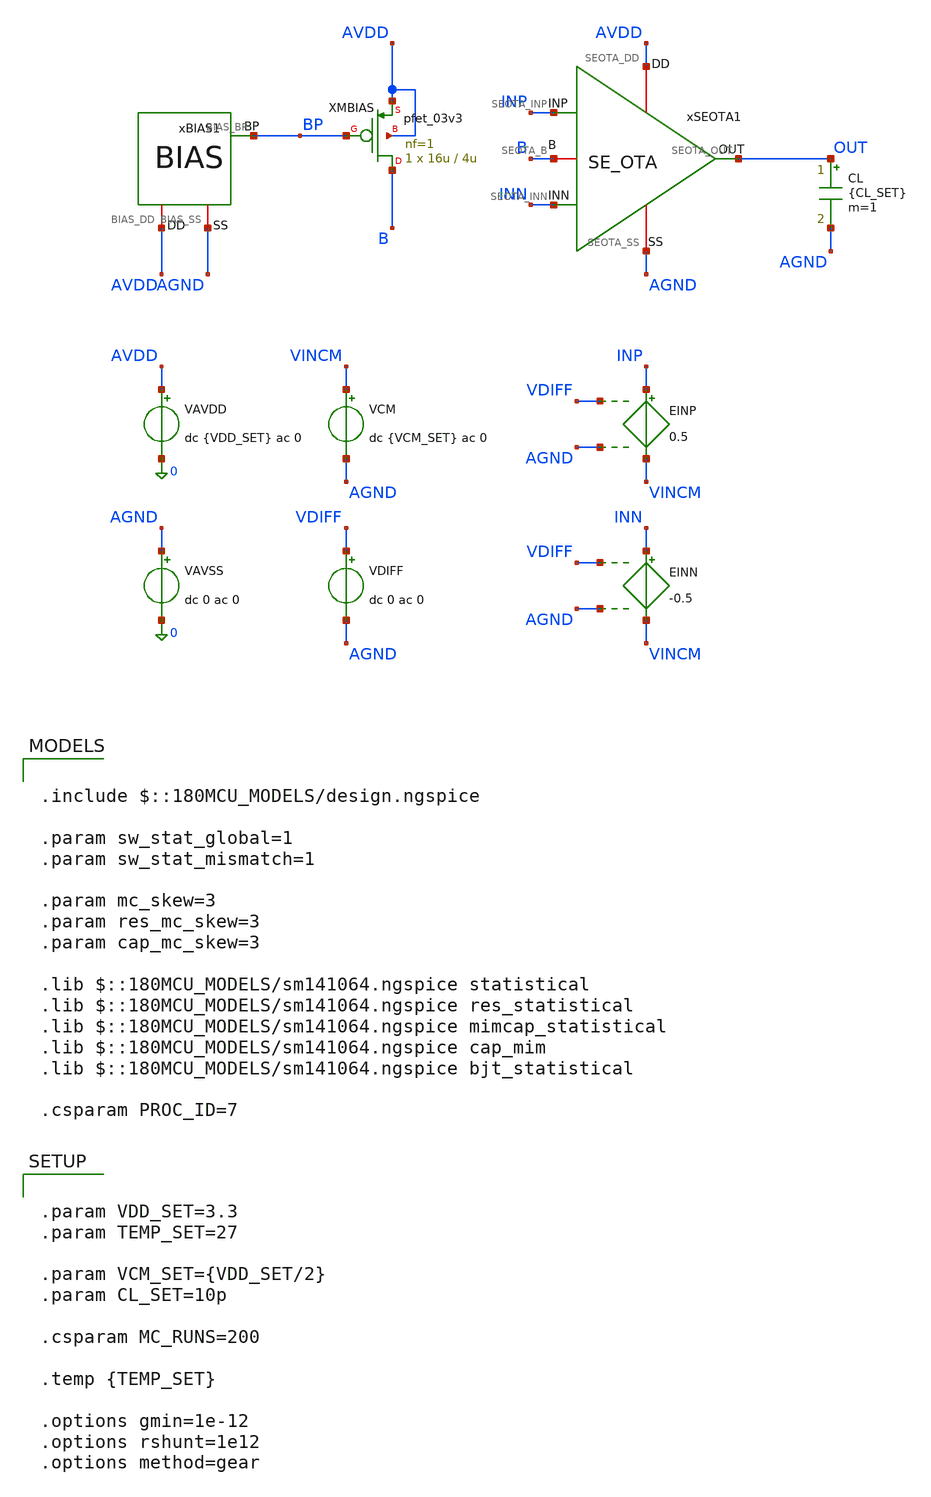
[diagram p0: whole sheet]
** sch_path: Design_Files/IC Design/Testbench/ANALOG_BLOCKS/SE_OTA/Open_Loop/SE_OTA_TB_OL_FULL.sch
**.subckt SE_OTA_TB_OL_FULL
VAVDD AVDD 0 dc {VDD_SET} ac 0
.save i(vavdd)
CL OUT AGND {CL_SET} m=1
VCM VINCM AGND dc {VCM_SET} ac 0
VDIFF VDIFF AGND dc 0 ac 0
xSEOTA1 AVDD AGND INP INN OUT B SE_OTA
VAVSS AGND 0 dc 0 ac 0
EINN INN VINCM VDIFF AGND -0.5
EINP INP VINCM VDIFF AGND 0.5
xBIAS1 AVDD AGND BP BIAS
XMBIAS B BP AVDD AVDD pfet_03v3 L=4u W=16u nf=1 ad='int((nf+1)/2) * W/nf * 0.18u' as='int((nf+2)/2) * W/nf * 0.18u'
+ pd='2*int((nf+1)/2) * (W/nf + 0.18u)' ps='2*int((nf+2)/2) * (W/nf + 0.18u)' nrd='0.18u / W' nrs='0.18u / W'
+ sa=0 sb=0 sd=0 m=1
**** begin user architecture code

.include $::180MCU_MODELS/design.ngspice

.param sw_stat_global=1
.param sw_stat_mismatch=1

.param mc_skew=3
.param res_mc_skew=3
.param cap_mc_skew=3

.lib $::180MCU_MODELS/sm141064.ngspice statistical
.lib $::180MCU_MODELS/sm141064.ngspice res_statistical
.lib $::180MCU_MODELS/sm141064.ngspice mimcap_statistical
.lib $::180MCU_MODELS/sm141064.ngspice cap_mim
.lib $::180MCU_MODELS/sm141064.ngspice bjt_statistical

.csparam PROC_ID=7




.control

destroy all

set noaskquit
set wr_singlescale
unset wr_vecnames

option klu
option numdgt=15
option method=gear
option maxord=2
option plotwinsize=0


if $&PROC_ID = 5
set proc=MM
else
if $&PROC_ID = 6
set proc=GL
else
set proc=FULL
end
end


shell mkdir -p /foss/designs/ECG_Acquisition_IC/Measurement_Results/IC_Simulation/ANALOG_BLOCKS/SE_OTA/{$proc}.Result_txt

shell rm -f /foss/designs/ECG_Acquisition_IC/Measurement_Results/IC_Simulation/ANALOG_BLOCKS/SE_OTA/{$proc}.Result_txt/{$proc}.ol_mc_summary.txt
shell rm -f /foss/designs/ECG_Acquisition_IC/Measurement_Results/IC_Simulation/ANALOG_BLOCKS/SE_OTA/{$proc}.Result_txt/{$proc}.ol_mc_debug_op.txt


echo run vos_V center_error_V ol_gain_1Hz ol_gain_dB ugf_Hz phase_ugf_deg pm_deg vout_center_V b_V ibias_A
+ idd_A power_W > /foss/designs/ECG_Acquisition_IC/Measurement_Results/IC_Simulation/ANALOG_BLOCKS/SE_OTA/{$proc}.Result_txt/{$proc}.ol_mc_summary.txt

echo run vos_V vout_zero_V vout_center_V center_error_V net1_V net2_V net3_V net4_V b_V ibias_A idd_A
+ power_W > /foss/designs/ECG_Acquisition_IC/Measurement_Results/IC_Simulation/ANALOG_BLOCKS/SE_OTA/{$proc}.Result_txt/{$proc}.ol_mc_debug_op.txt


let run=1
let mc_runs=$&MC_RUNS


dowhile run <= mc_runs


set runnum=$&run

setseed $runnum
mc_source


option klu
option numdgt=15
option method=gear
option maxord=2
option plotwinsize=0


* DEFAULT VALUES

set vos_val=0
set vout_zero_val=0
set vout_center_val=0
set center_error_val=0

set gain_val=0
set gain_db_val=0
set ugf_val=0
set phase_val=0
set pm_val=0

set net1_val=0
set net2_val=0
set net3_val=0
set net4_val=0

set b_val=0
set ibias_val=0
set idd_val=0
set power_val=0


* INITIAL SOURCES

alter @VCM[DC]=1.65
alter @VDIFF[DC]=0

alter @VCM[ACMAG]=0
alter @VDIFF[ACMAG]=0
alter @VAVDD[ACMAG]=0
alter @VAVSS[ACMAG]=0


save all
save @m.xmbias.m0[id]


* ZERO-DIFFERENTIAL OP

op

let vout_zero=v(OUT)-v(AGND)

set vout_zero_val=$&vout_zero


destroy all


* FIND OFFSET

alter @VDIFF[DC]=0

dc VDIFF -50m 50m 10u

meas dc vos_center when v(OUT)=1.65 cross=1

set vos_val=$&vos_center


destroy all


* CENTER OTA

alter @VDIFF[DC]=$vos_val

alter @VCM[ACMAG]=0
alter @VDIFF[ACMAG]=0
alter @VAVDD[ACMAG]=0
alter @VAVSS[ACMAG]=0


save all
save @m.xmbias.m0[id]


op


let vout_center=v(OUT)-v(AGND)
let center_error=vout_center-1.65

let b_op=v(B)-v(AGND)

let net1_op=v(xseota1.net1)-v(AGND)
let net2_op=v(xseota1.net2)-v(AGND)
let net3_op=v(xseota1.net3)-v(AGND)
let net4_op=v(xseota1.net4)-v(AGND)

let ibias=abs(@m.xmbias.m0[id])
let idd_total=abs(vavdd#branch)
let power_total=(v(AVDD)-v(AGND))*idd_total


set vout_center_val=$&vout_center
set center_error_val=$&center_error

set b_val=$&b_op

set net1_val=$&net1_op
set net2_val=$&net2_op
set net3_val=$&net3_op
set net4_val=$&net4_op

set ibias_val=$&ibias
set idd_val=$&idd_total
set power_val=$&power_total


echo $runnum $vos_val $vout_zero_val $vout_center_val $center_error_val $net1_val $net2_val $net3_val
+ $net4_val $b_val $ibias_val $idd_val $power_val >> /foss/designs/ECG_Acquisition_IC/Measurement_Results/IC_Simulation/ANALOG_BLOCKS/SE_OTA/{$proc}.Result_txt/{$proc}.ol_mc_debug_op.txt


destroy all


* OPEN-LOOP AC AT CENTERED OP

alter @VDIFF[DC]=$vos_val

alter @VCM[ACMAG]=0
alter @VDIFF[ACMAG]=1
alter @VDIFF[ACPHASE]=0
alter @VAVDD[ACMAG]=0
alter @VAVSS[ACMAG]=0


ac dec 200 0.01 1G


let vin_diff=v(INP)-v(INN)
let vout_ac=v(OUT)-v(AGND)

let ol_tf=vout_ac/vin_diff

let ol_gain=mag(ol_tf)
let ol_gain_db=db(ol_tf)
let ol_phase=(180/3.141592653589793)*cph(ol_tf)


meas ac ol_gain_1 find ol_gain at=1
meas ac ol_gain_db_1 find ol_gain_db at=1

set gain_val=$&ol_gain_1
set gain_db_val=$&ol_gain_db_1


meas ac ugf_meas when ol_gain=1 cross=1

set ugf_val=$&ugf_meas


meas ac phase_ugf find ol_phase at=$ugf_val

set phase_val=$&phase_ugf


let pm_calc=180+phase_ugf

set pm_val=$&pm_calc


echo $runnum $vos_val $center_error_val $gain_val $gain_db_val $ugf_val $phase_val $pm_val $vout_center_val
+ $b_val $ibias_val $idd_val $power_val >> /foss/designs/ECG_Acquisition_IC/Measurement_Results/IC_Simulation/ANALOG_BLOCKS/SE_OTA/{$proc}.Result_txt/{$proc}.ol_mc_summary.txt


destroy all

let run=run+1


end


quit

.endc




.param VDD_SET=3.3
.param TEMP_SET=27

.param VCM_SET={VDD_SET/2}
.param CL_SET=10p

.csparam MC_RUNS=200

.temp {TEMP_SET}

.options gmin=1e-12
.options rshunt=1e12
.options method=gear


**** end user architecture code
**.ends

* expanding   symbol:  ECG_Acquisition_IC/Design_Files/IC
*+ Design/Schematic/ANALOG_BLOCKS/SE_OTA/SE_OTA.sym # of pins=6
** sym_path: Design_Files/IC Design/Schematic/SE_OTA/SE_OTA.sym
** sch_path: Design_Files/IC Design/Schematic/SE_OTA/SE_OTA.sch
.subckt SE_OTA SEOTA_DD SEOTA_SS SEOTA_INP SEOTA_INN SEOTA_OUT SEOTA_B
*.iopin SEOTA_DD
*.iopin SEOTA_SS
*.ipin SEOTA_INP
*.ipin SEOTA_INN
*.opin SEOTA_OUT
*.iopin SEOTA_B
XM3 net4 net4 SEOTA_DD SEOTA_DD pfet_03v3 L=4u W=1u nf=1 ad='int((nf+1)/2) * W/nf * 0.18u' as='int((nf+2)/2) * W/nf * 0.18u'
+ pd='2*int((nf+1)/2) * (W/nf + 0.18u)' ps='2*int((nf+2)/2) * (W/nf + 0.18u)' nrd='0.18u / W' nrs='0.18u / W'
+ sa=0 sb=0 sd=0 m=60
XM7 SEOTA_OUT SEOTA_B SEOTA_SS SEOTA_SS nfet_03v3 L=0.5u W=1u nf=1 ad='int((nf+1)/2) * W/nf * 0.18u'
+ as='int((nf+2)/2) * W/nf * 0.18u' pd='2*int((nf+1)/2) * (W/nf + 0.18u)' ps='2*int((nf+2)/2) * (W/nf + 0.18u)'
+ nrd='0.18u / W' nrs='0.18u / W' sa=0 sb=0 sd=0 m=100
Rz net1 net2 3.8k m=1
XM5 net3 SEOTA_B SEOTA_SS SEOTA_SS nfet_03v3 L=2u W=1u nf=1 ad='int((nf+1)/2) * W/nf * 0.18u' as='int((nf+2)/2) * W/nf * 0.18u'
+ pd='2*int((nf+1)/2) * (W/nf + 0.18u)' ps='2*int((nf+2)/2) * (W/nf + 0.18u)' nrd='0.18u / W' nrs='0.18u / W'
+ sa=0 sb=0 sd=0 m=10
XM6 SEOTA_OUT net1 SEOTA_DD SEOTA_DD pfet_03v3 L=0.5u W=1u nf=1 ad='int((nf+1)/2) * W/nf * 0.18u' as='int((nf+2)/2) * W/nf * 0.18u'
+ pd='2*int((nf+1)/2) * (W/nf + 0.18u)' ps='2*int((nf+2)/2) * (W/nf + 0.18u)' nrd='0.18u / W' nrs='0.18u / W'
+ sa=0 sb=0 sd=0 m=400
XM8 SEOTA_B SEOTA_B SEOTA_SS SEOTA_SS nfet_03v3 L=2u W=1u nf=1 ad='int((nf+1)/2) * W/nf * 0.18u' as='int((nf+2)/2) * W/nf * 0.18u'
+ pd='2*int((nf+1)/2) * (W/nf + 0.18u)' ps='2*int((nf+2)/2) * (W/nf + 0.18u)' nrd='0.18u / W' nrs='0.18u / W'
+ sa=0 sb=0 sd=0 m=20
Cc net2 SEOTA_OUT 2p m=1
XM4 net1 net4 SEOTA_DD SEOTA_DD pfet_03v3 L=4u W=1u nf=1 ad='int((nf+1)/2) * W/nf * 0.18u' as='int((nf+2)/2) * W/nf * 0.18u'
+ pd='2*int((nf+1)/2) * (W/nf + 0.18u)' ps='2*int((nf+2)/2) * (W/nf + 0.18u)' nrd='0.18u / W' nrs='0.18u / W'
+ sa=0 sb=0 sd=0 m=60
XM1 net4 SEOTA_INN net3 SEOTA_SS nfet_03v3 L=4u W=1u nf=1 ad='int((nf+1)/2) * W/nf * 0.18u' as='int((nf+2)/2) * W/nf * 0.18u'
+ pd='2*int((nf+1)/2) * (W/nf + 0.18u)' ps='2*int((nf+2)/2) * (W/nf + 0.18u)' nrd='0.18u / W' nrs='0.18u / W'
+ sa=0 sb=0 sd=0 m=400
XM2 net1 SEOTA_INP net3 SEOTA_SS nfet_03v3 L=4u W=1u nf=1 ad='int((nf+1)/2) * W/nf * 0.18u' as='int((nf+2)/2) * W/nf * 0.18u'
+ pd='2*int((nf+1)/2) * (W/nf + 0.18u)' ps='2*int((nf+2)/2) * (W/nf + 0.18u)' nrd='0.18u / W' nrs='0.18u / W'
+ sa=0 sb=0 sd=0 m=400
.ends


* expanding   symbol:  ECG_Acquisition_IC/Design_Files/IC Design/Schematic/AFE_BLOCKS/BIAS/BIAS.sym
*+ # of pins=3
** sym_path: Design_Files/IC Design/Schematic/AFE_BLOCKS/BIAS/BIAS.sym
** sch_path: Design_Files/IC Design/Schematic/AFE_BLOCKS/BIAS/BIAS.sch
.subckt BIAS BIAS_DD BIAS_SS BIAS_BP
*.iopin BIAS_DD
*.iopin BIAS_SS
*.opin BIAS_BP
XMN2 BIAS_BP net2 net1 BIAS_SS nfet_03v3 L=4u W=16u nf=1 ad='int((nf+1)/2) * W/nf * 0.18u' as='int((nf+2)/2) * W/nf * 0.18u'
+ pd='2*int((nf+1)/2) * (W/nf + 0.18u)' ps='2*int((nf+2)/2) * (W/nf + 0.18u)' nrd='0.18u / W' nrs='0.18u / W'
+ sa=0 sb=0 sd=0 m=1
XMP2 BIAS_BP BIAS_BP BIAS_DD BIAS_DD pfet_03v3 L=4u W=16u nf=1 ad='int((nf+1)/2) * W/nf * 0.18u' as='int((nf+2)/2) * W/nf * 0.18u'
+ pd='2*int((nf+1)/2) * (W/nf + 0.18u)' ps='2*int((nf+2)/2) * (W/nf + 0.18u)' nrd='0.18u / W' nrs='0.18u / W'
+ sa=0 sb=0 sd=0 m=1
XMN1 net2 net2 net3 BIAS_SS nfet_03v3 L=4u W=24u nf=1 ad='int((nf+1)/2) * W/nf * 0.18u' as='int((nf+2)/2) * W/nf * 0.18u'
+ pd='2*int((nf+1)/2) * (W/nf + 0.18u)' ps='2*int((nf+2)/2) * (W/nf + 0.18u)' nrd='0.18u / W' nrs='0.18u / W'
+ sa=0 sb=0 sd=0 m=1
XMP1 net2 BIAS_BP BIAS_DD BIAS_DD pfet_03v3 L=4u W=16u nf=1 ad='int((nf+1)/2) * W/nf * 0.18u' as='int((nf+2)/2) * W/nf * 0.18u'
+ pd='2*int((nf+1)/2) * (W/nf + 0.18u)' ps='2*int((nf+2)/2) * (W/nf + 0.18u)' nrd='0.18u / W' nrs='0.18u / W'
+ sa=0 sb=0 sd=0 m=1
XMST BIAS_BP BIAS_BP net2 BIAS_SS nfet_03v3 L=10u W=0.5u nf=1 ad='int((nf+1)/2) * W/nf * 0.18u' as='int((nf+2)/2) * W/nf * 0.18u'
+ pd='2*int((nf+1)/2) * (W/nf + 0.18u)' ps='2*int((nf+2)/2) * (W/nf + 0.18u)' nrd='0.18u / W' nrs='0.18u / W'
+ sa=0 sb=0 sd=0 m=1
XQ1 BIAS_SS BIAS_SS net3 pnp_05p00x00p42 m=1 par=1
XQ2 BIAS_SS BIAS_SS net4 pnp_05p00x00p42 m=30 par=30
XRS net4 net1 BIAS_SS nwell r_width=3e-6 r_length=1.522e-6 m=1
.ends

.end
